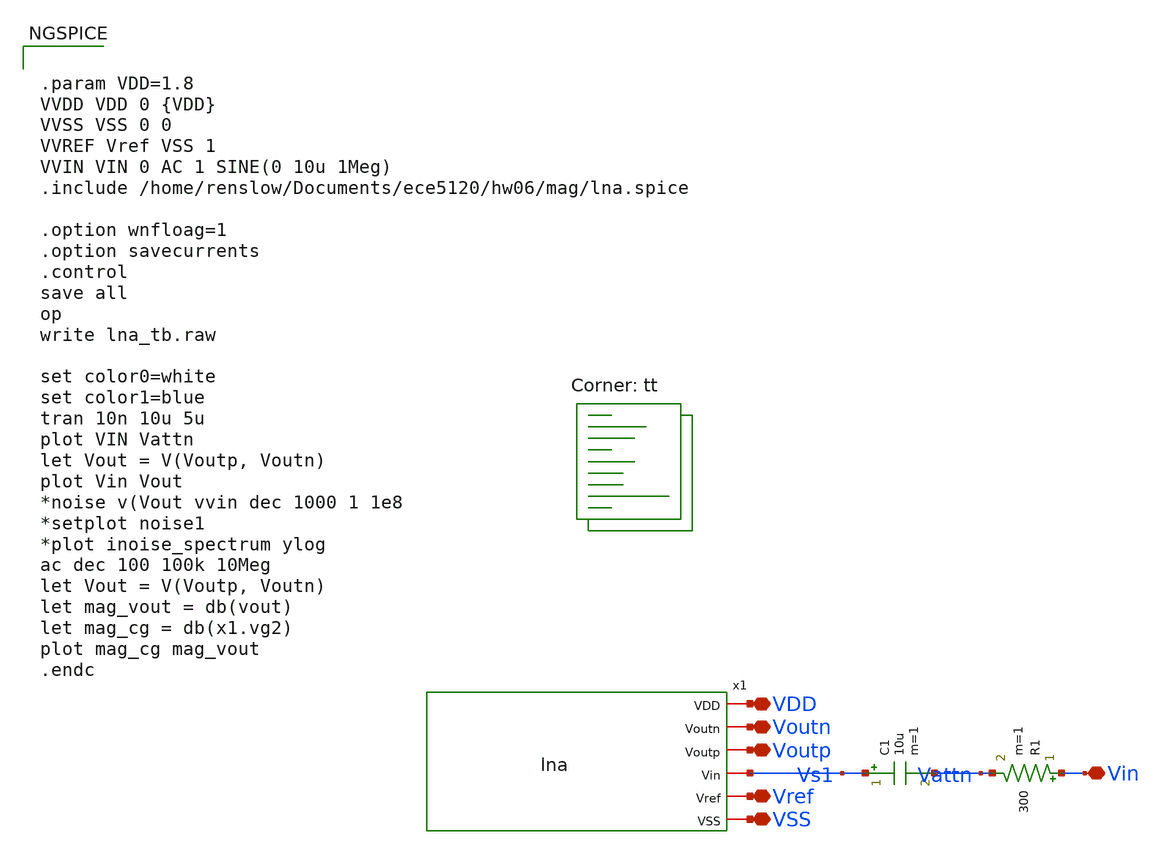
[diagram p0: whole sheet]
** sch_path: hw06/mag/lna_tb.sch
**.subckt lna_tb VDD Voutn Voutp Vin Vref VSS
*.iopin VDD
*.iopin Voutn
*.iopin Voutp
*.iopin Vin
*.iopin Vref
*.iopin VSS
x1 VDD Voutn Voutp Vs1 Vref VSS lna
C1 Vs1 Vattn 10u m=1
R1 Vin Vattn 300 m=1
**** begin user architecture code
.lib $::SKYWATER_MODELS/sky130.lib.spice tt


.param VDD=1.8
VVDD VDD 0 {VDD}
VVSS VSS 0 0
VVREF Vref VSS 1
VVIN VIN 0 AC 1 SINE(0 10u 1Meg)
.include /home/renslow/Documents/ece5120/hw06/mag/lna.spice

.option wnfloag=1
.option savecurrents
.control
save all
op
write lna_tb.raw

set color0=white
set color1=blue
tran 10n 10u 5u
plot VIN Vattn
let Vout = V(Voutp, Voutn)
plot Vin Vout
*noise v(Vout vvin dec 1000 1 1e8
*setplot noise1
*plot inoise_spectrum ylog
ac dec 100 100k 10Meg
let Vout = V(Voutp, Voutn)
let mag_vout = db(vout)
let mag_cg = db(x1.vg2)
plot mag_cg mag_vout
.endc


**** end user architecture code
**.ends
.end
